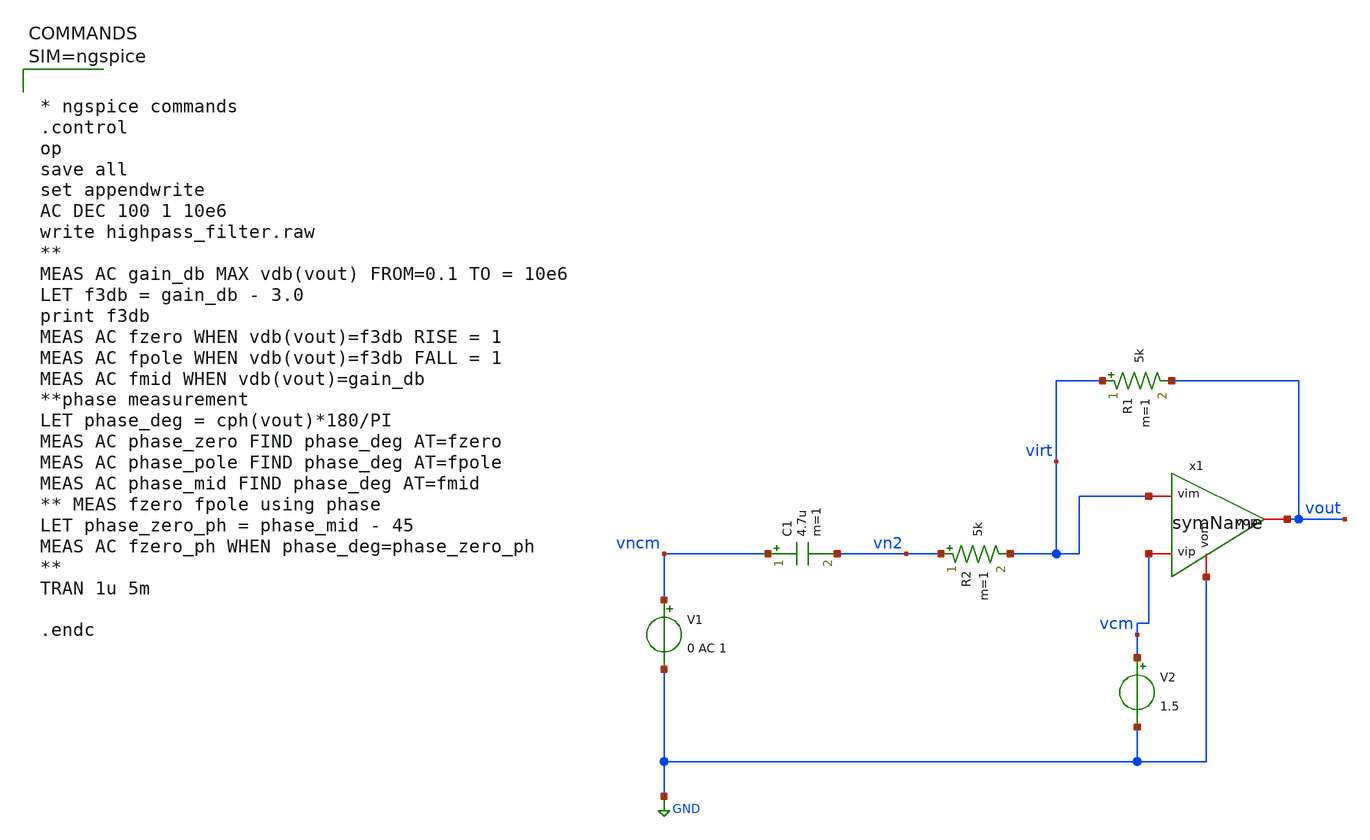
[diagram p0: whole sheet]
** sch_path: xschem/highpass_filter.sch
**.subckt highpass_filter
V1 vncm GND 0 AC 1
C1 vncm vn2 4.7u m=1
R2 vn2 virt 5k m=1
R1 virt vout 5k m=1
V2 vcm GND 1.5
x1 vout vcm virt GND symName
**** begin user architecture code



* ngspice commands
.control
op
save all
set appendwrite
AC DEC 100 1 10e6
write highpass_filter.raw
**
MEAS AC gain_db MAX vdb(vout) FROM=0.1 TO = 10e6
LET f3db = gain_db - 3.0
print f3db
MEAS AC fzero WHEN vdb(vout)=f3db RISE = 1
MEAS AC fpole WHEN vdb(vout)=f3db FALL = 1
MEAS AC fmid WHEN vdb(vout)=gain_db
**phase measurement
LET phase_deg = cph(vout)*180/PI
MEAS AC phase_zero FIND phase_deg AT=fzero
MEAS AC phase_pole FIND phase_deg AT=fpole
MEAS AC phase_mid FIND phase_deg AT=fmid
** MEAS fzero fpole using phase
LET phase_zero_ph = phase_mid - 45
MEAS AC fzero_ph WHEN phase_deg=phase_zero_ph
**
TRAN 1u 5m

.endc



**** end user architecture code
**.ends

* expanding   symbol:  symName.sym # of pins=4
** sym_path: xschem/symName.sym
** sch_path: xschem/symName.sch
.subckt symName vop vip vim vom
*.iopin vop
*.iopin vom
*.iopin vip
*.iopin vim
E1 vop vom vip vim 1000
.ends

.GLOBAL GND
.end
